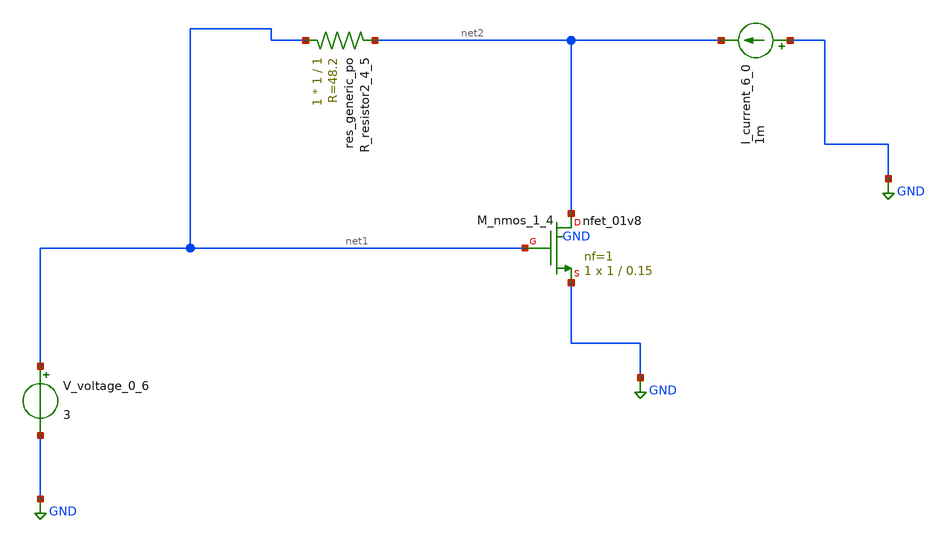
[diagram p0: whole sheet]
** sch_path: schematics/AMSNet/447.sch
**.subckt 447
I_current_6_0 GND net2 1m
XM_nmos_1_4 net2 net1 GND GND sky130_fd_pr__nfet_01v8 L=0.15 W=1 nf=1 ad='int((1 + 1)/2) * 1 / 1 * 0.29'
+ as='int((1 + 2)/2) * 1 / 1 * 0.29' pd='2*int((1 + 1)/2) * (1 / 1 + 0.29)' ps='2*int((1 + 2)/2) * (1 / 1 + 0.29)'
+ nrd='0.29 / 1 ' nrs='0.29 / 1 ' sa=0 sb=0 sd=0 mult=1 m=1
XR_resistor2_4_5 net1 net2 sky130_fd_pr__res_generic_po W=1 L=1 m=1
V_voltage_0_6 net1 GND 3
**.ends
.GLOBAL GND
.end
